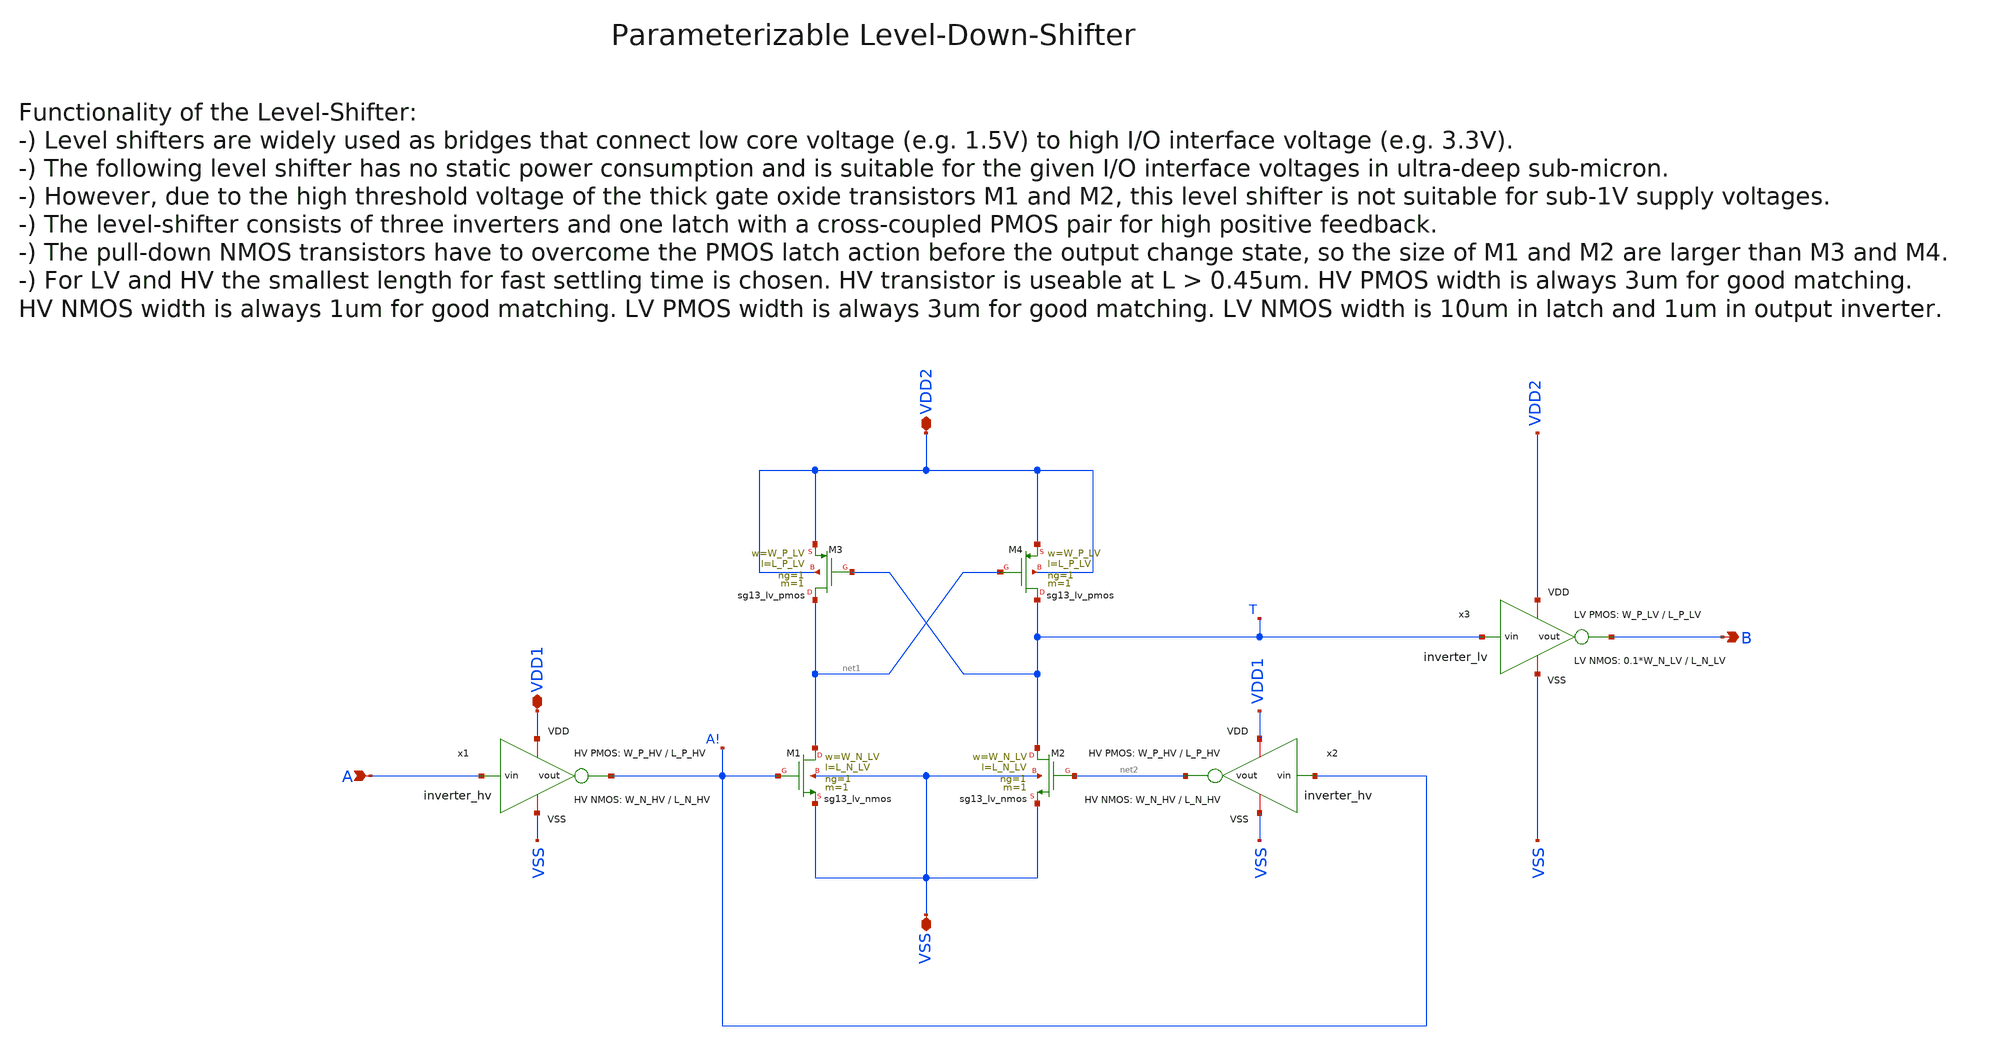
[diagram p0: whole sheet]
** sch_path: SG13G2_ATBS-ADC-main/xschem/level_shifter/level_down_shifter.sch
**.subckt level_down_shifter A VDD1 VSS B VDD2
*.ipin A
*.iopin VDD1
*.iopin VSS
*.opin B
*.iopin VDD2
x3 VDD2 T B VSS inverter_lv W_P=W_P_LV L_P=L_P_LV W_N=0.1*W_N_LV L_N=L_N_LV
x1 VDD1 A A! VSS inverter_hv W_P=W_P_HV L_P=L_P_HV W_N=W_N_HV L_N=L_N_HV
x2 VDD1 A! net2 VSS inverter_hv W_P=W_P_HV L_P=L_P_HV W_N=W_N_HV L_N=L_N_HV
XM1 net1 A! VSS VSS sg13_lv_nmos w=W_N_LV l=L_N_LV ng=1 m=1 mm_ok=1
XM3 net1 T VDD2 VDD2 sg13_lv_pmos w=W_P_LV l=L_P_LV ng=1 m=1 mm_ok=1
XM2 T net2 VSS VSS sg13_lv_nmos w=W_N_LV l=L_N_LV ng=1 m=1 mm_ok=1
XM4 T net1 VDD2 VDD2 sg13_lv_pmos w=W_P_LV l=L_P_LV ng=1 m=1 mm_ok=1
**.ends

* expanding   symbol:  inverter/inverter_lv.sym # of pins=4
** sym_path: SG13G2_ATBS-ADC-main/xschem/inverter/inverter_lv.sym
** sch_path: SG13G2_ATBS-ADC-main/xschem/inverter/inverter_lv.sch
.subckt inverter_lv VDD vin vout VSS  W_P=3.0u L_P=0.13u W_N=1.0u L_N=0.13u
*.ipin vin
*.iopin VDD
*.iopin VSS
*.opin vout
XM1 vout vin VDD VDD sg13_lv_pmos w=W_P l=L_P ng=1 m=1 mm_ok=1
XM2 vout vin VSS VSS sg13_lv_nmos w=W_N l=L_N ng=1 m=1 mm_ok=1
.ends


* expanding   symbol:  inverter/inverter_hv.sym # of pins=4
** sym_path: SG13G2_ATBS-ADC-main/xschem/inverter/inverter_hv.sym
** sch_path: SG13G2_ATBS-ADC-main/xschem/inverter/inverter_hv.sch
.subckt inverter_hv VDD vin vout VSS  W_P=3.0u L_P=0.50u W_N=1.0u L_N=0.50u
*.ipin vin
*.iopin VDD
*.iopin VSS
*.opin vout
XM1 vout vin VDD VDD sg13_hv_pmos w=W_P l=L_P ng=1 m=1 mm_ok=1
XM2 vout vin VSS VSS sg13_hv_nmos w=W_N l=L_N ng=1 m=1 mm_ok=1
.ends

.end
